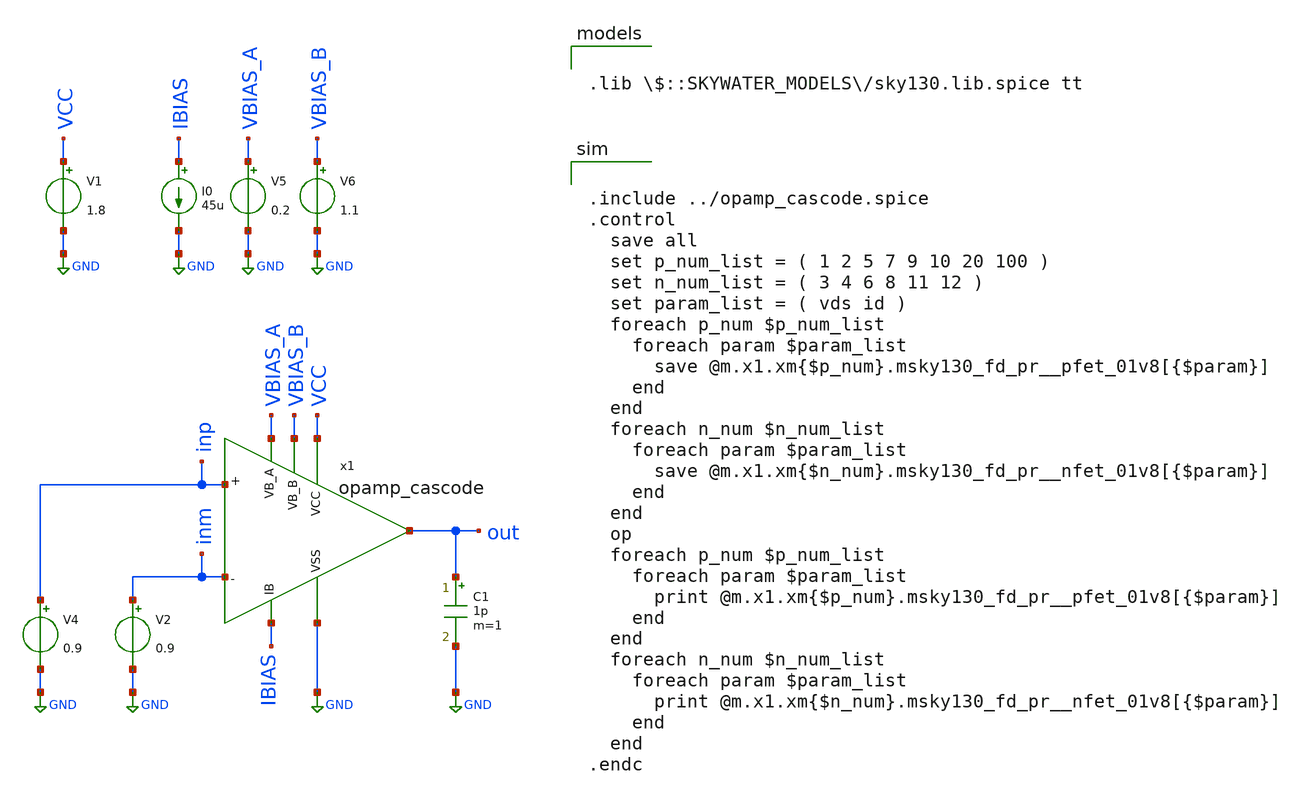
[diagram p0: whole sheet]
** sch_path: 06_ParasiticsSim/opamp_cascode_op_point.sch
**.subckt opamp_cascode_op_point
V1 VCC GND 1.8
V4 inp GND 0.9
V2 inm GND 0.9
C1 out GND 1p m=1
V5 VBIAS_A GND 0.2
V6 VBIAS_B GND 1.1
I0 IBIAS GND 45u
x1 inp inm VCC GND out VBIAS_A VBIAS_B IBIAS opamp_cascode
**** begin user architecture code


.include ../opamp_cascode.spice
.control
  save all
  set p_num_list = ( 1 2 5 7 9 10 20 100 )
  set n_num_list = ( 3 4 6 8 11 12 )
  set param_list = ( vds id )
  foreach p_num $p_num_list
    foreach param $param_list
      save @m.x1.xm{$p_num}.msky130_fd_pr__pfet_01v8[{$param}]
    end
  end
  foreach n_num $n_num_list
    foreach param $param_list
      save @m.x1.xm{$n_num}.msky130_fd_pr__nfet_01v8[{$param}]
    end
  end
  op
  foreach p_num $p_num_list
    foreach param $param_list
      print @m.x1.xm{$p_num}.msky130_fd_pr__pfet_01v8[{$param}]
    end
  end
  foreach n_num $n_num_list
    foreach param $param_list
      print @m.x1.xm{$n_num}.msky130_fd_pr__nfet_01v8[{$param}]
    end
  end
.endc



.lib $::SKYWATER_MODELS/sky130.lib.spice tt

**** end user architecture code
**.ends
.GLOBAL GND
.end
